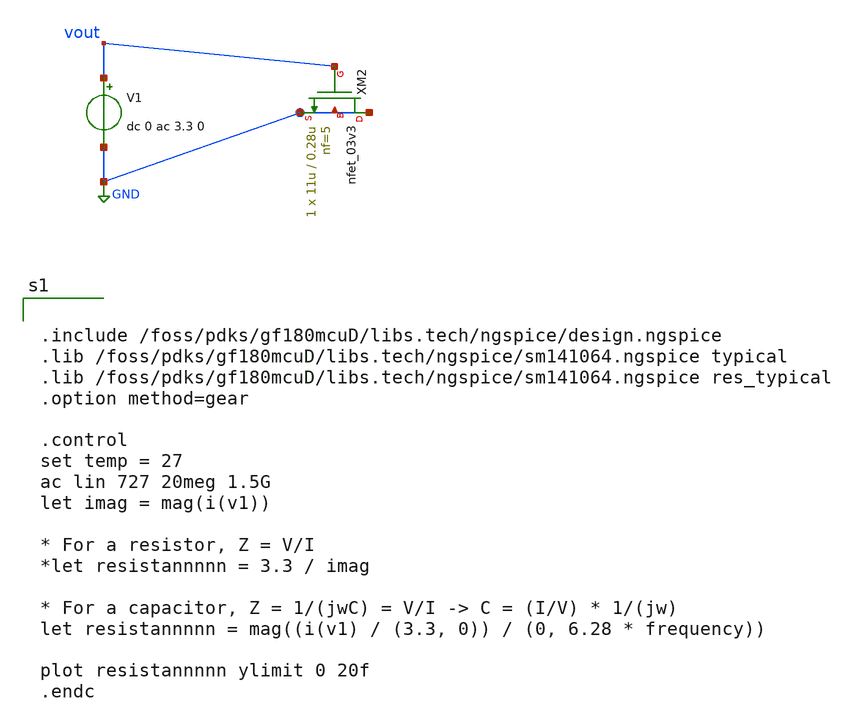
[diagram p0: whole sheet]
** sch_path: blocks/vga/untitled.sch
**.subckt untitled
V1 vout GND dc 0 ac 3.3 0
.save i(v1)
XM2 GND vout GND GND nfet_03v3 L=0.28u W=11u nf=5 ad='int((nf+1)/2) * W/nf * 0.18u' as='int((nf+2)/2) * W/nf * 0.18u'
+ pd='2*int((nf+1)/2) * (W/nf + 0.18u)' ps='2*int((nf+2)/2) * (W/nf + 0.18u)' nrd='0.18u / W' nrs='0.18u / W'
+ sa=0 sb=0 sd=0 m=1
**** begin user architecture code


.include /foss/pdks/gf180mcuD/libs.tech/ngspice/design.ngspice
.lib /foss/pdks/gf180mcuD/libs.tech/ngspice/sm141064.ngspice typical
.lib /foss/pdks/gf180mcuD/libs.tech/ngspice/sm141064.ngspice res_typical
.option method=gear

.control
set temp = 27
ac lin 727 20meg 1.5G
let imag = mag(i(v1))

* For a resistor, Z = V/I
*let resistannnnn = 3.3 / imag

* For a capacitor, Z = 1/(jwC) = V/I -> C = (I/V) * 1/(jw)
let resistannnnn = mag((i(v1) / (3.3, 0)) / (0, 6.28 * frequency))

plot resistannnnn ylimit 0 20f
.endc


**** end user architecture code
**.ends
.GLOBAL GND
.end
